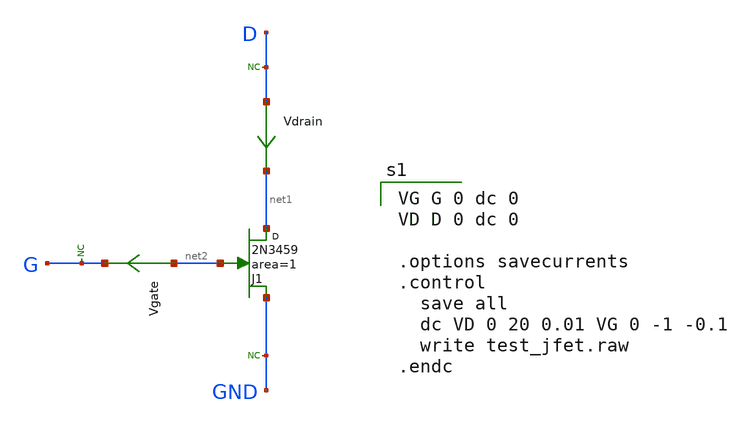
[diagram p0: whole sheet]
** sch_path: xschem_library/examples/test_jfet.sch
**.subckt test_jfet
J1 net1 net2 GND 2N3459 area=1 m=1
* noconn GND
* noconn D
* noconn G
Vgate net2 G 0
.save i(vgate)
Vdrain D net1 0
.save i(vdrain)
**** begin user architecture code

VG G 0 dc 0
VD D 0 dc 0

.options savecurrents
.control
  save all
  dc VD 0 20 0.01 VG 0 -1 -0.1
  write test_jfet.raw
.endc


.MODEL 2N3459 NJF(VTO=-1.4 BETA=1.265m BETATCE=-0.5 LAMBDA=4m RD=1 RS=1 CGS=2.916p CGD=2.8p PB=0.5
+ IS=114.5f XTI=3 AF=1 FC=0.5 N=1 NR=2)

**** end user architecture code
**.ends
.end
